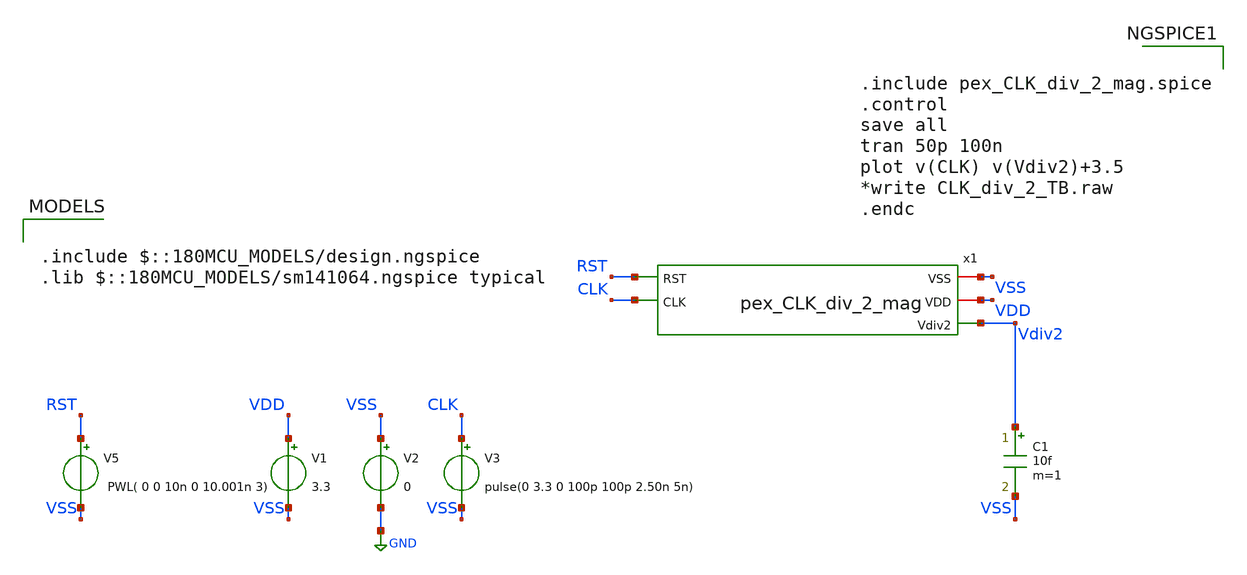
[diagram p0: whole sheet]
** sch_path: Clock_Generator_PAKISTAN_02/xschem/pex_CLK_div_2_mag_TB.sch
**.subckt pex_CLK_div_2_mag_TB
V1 VDD VSS 3.3
V2 VSS GND 0
V3 CLK VSS pulse(0 3.3 0 100p 100p 2.50n 5n)
C1 Vdiv2 VSS 10f m=1
V5 RST VSS PWL( 0 0 10n 0 10.001n 3)
x1 VSS VDD Vdiv2 RST CLK pex_CLK_div_2_mag
**** begin user architecture code

.include $::180MCU_MODELS/design.ngspice
.lib $::180MCU_MODELS/sm141064.ngspice typical



.include pex_CLK_div_2_mag.spice
.control
save all
tran 50p 100n
plot v(CLK) v(Vdiv2)+3.5
*write CLK_div_2_TB.raw
.endc


**** end user architecture code
**.ends
.GLOBAL GND
.end
